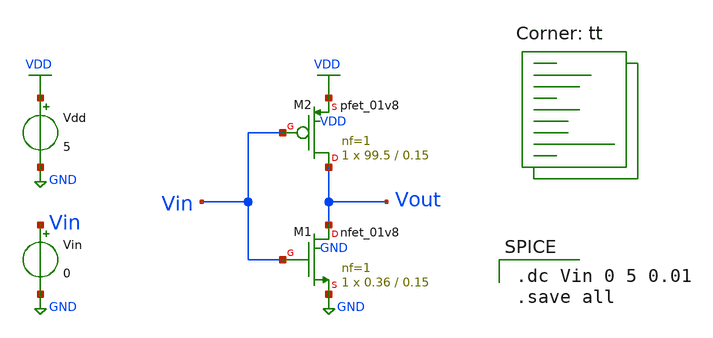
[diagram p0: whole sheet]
** sch_path: inverter.sch
**.subckt inverter
Vdd VDD GND 5
XM1 Vout Vin GND GND sky130_fd_pr__nfet_01v8 L=0.15 W=0.36 nf=1 ad='int((nf+1)/2) * W/nf * 0.29' as='int((nf+2)/2) * W/nf * 0.29'
+ pd='2*int((nf+1)/2) * (W/nf + 0.29)' ps='2*int((nf+2)/2) * (W/nf + 0.29)' nrd='0.29 / W' nrs='0.29 / W'
+ sa=0 sb=0 sd=0 mult=1 m=1
XM2 Vout Vin VDD VDD sky130_fd_pr__pfet_01v8 L=0.15 W=99.5 nf=1 ad='int((nf+1)/2) * W/nf * 0.29' as='int((nf+2)/2) * W/nf * 0.29'
+ pd='2*int((nf+1)/2) * (W/nf + 0.29)' ps='2*int((nf+2)/2) * (W/nf + 0.29)' nrd='0.29 / W' nrs='0.29 / W'
+ sa=0 sb=0 sd=0 mult=1 m=1
Vin Vin GND 0
**** begin user architecture code

.dc Vin 0 5 0.01
.save all

.lib $::SKYWATER_MODELS/sky130.lib.spice tt
**** end user architecture code
**.ends
.GLOBAL VDD
.GLOBAL GND
.end
